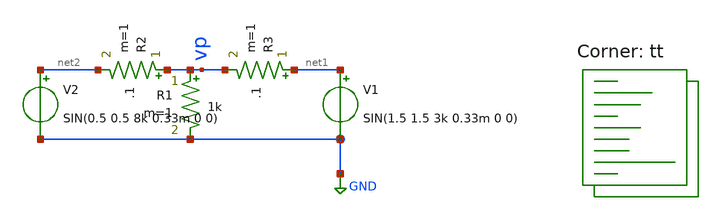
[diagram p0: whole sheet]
** sch_path: Schematics/test_graphs.sch
**.subckt test_graphs
V1 net1 GND SIN(1.5 1.5 3k 0.33m 0 0)
R1 vp GND 1k m=1
V2 net2 GND SIN(0.5 0.5 8k 0.33m 0 0)
R2 vp net2 .1 m=1
R3 net1 vp .1 m=1
**** begin user architecture code
.lib $::SKYWATER_MODELS/sky130.lib.spice tt
**** end user architecture code
**.ends
.GLOBAL GND
**** begin user architecture code

.options savecurrents
.tran 100n 1m uic
.save all
.control
	run
	write test_graphs.raw
*plot all.Vout
.endc


**** end user architecture code
.end
